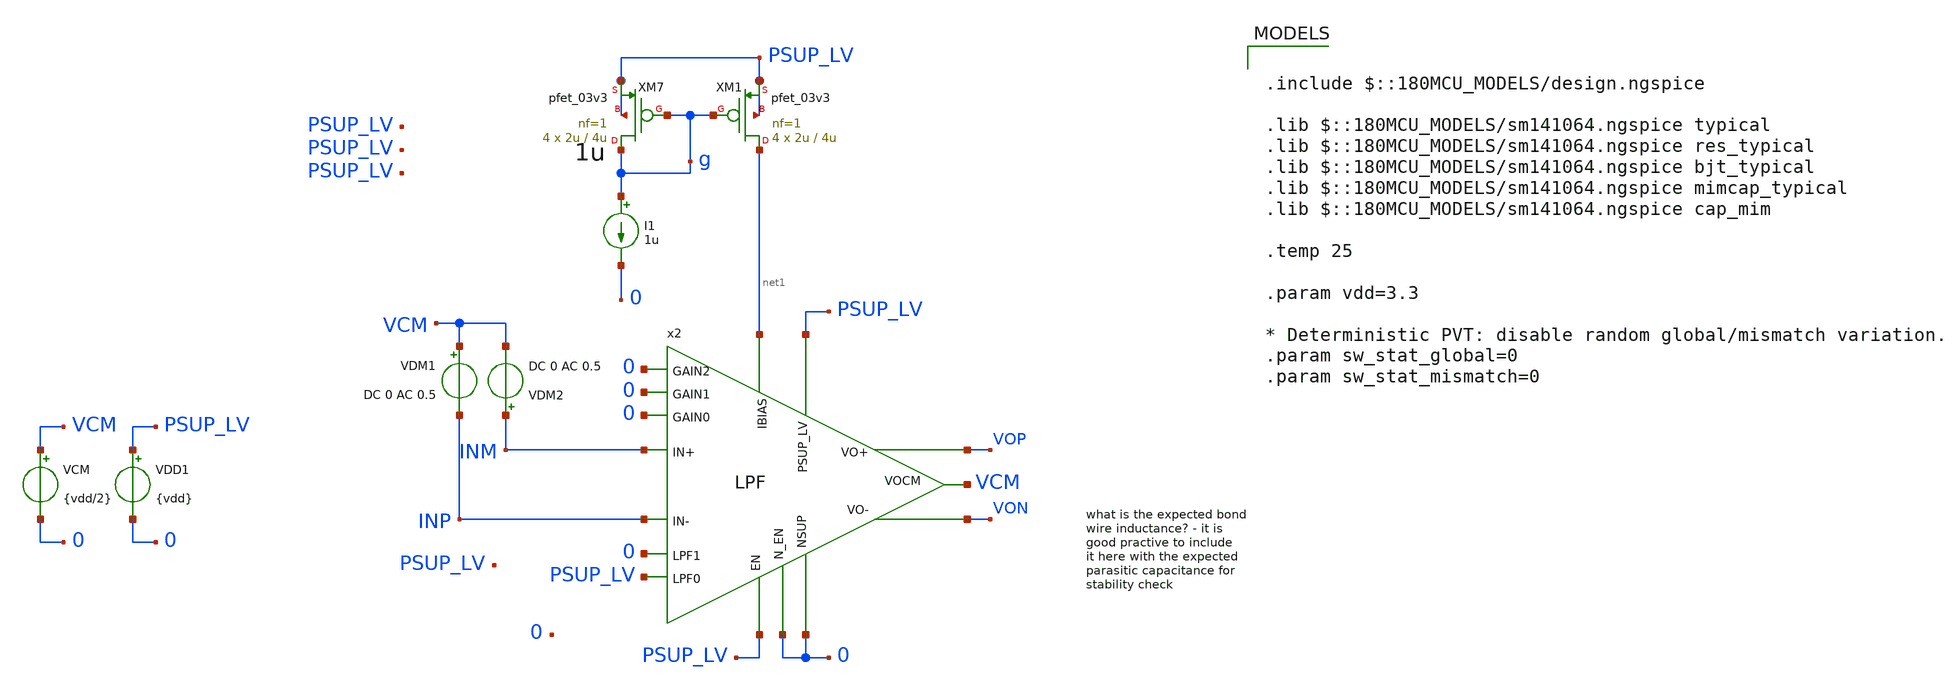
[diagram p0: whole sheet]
** sch_path: xschem/blocks/LPF/tb_LPF_gain.sch
**.subckt tb_LPF_gain
VDD1 PSUP_LV 0 {vdd}
VCM VCM 0 {vdd/2}
VDM2 INM VCM DC 0 AC 0.5
VDM1 VCM INP DC 0 AC 0.5
x2 PSUP_LV 0 PSUP_LV 0 net1 0 0 0 0 PSUP_LV INM VOP VCM INP VON LPF
XM7 g g PSUP_LV PSUP_LV pfet_03v3 L=4u W=2u nf=1 ad='int((nf+1)/2) * W/nf * 0.18u' as='int((nf+2)/2) * W/nf * 0.18u'
+ pd='2*int((nf+1)/2) * (W/nf + 0.18u)' ps='2*int((nf+2)/2) * (W/nf + 0.18u)' nrd='0.18u / W' nrs='0.18u / W'
+ sa=0 sb=0 sd=0 m=4
XM1 net1 g PSUP_LV PSUP_LV pfet_03v3 L=4u W=2u nf=1 ad='int((nf+1)/2) * W/nf * 0.18u' as='int((nf+2)/2) * W/nf * 0.18u'
+ pd='2*int((nf+1)/2) * (W/nf + 0.18u)' ps='2*int((nf+2)/2) * (W/nf + 0.18u)' nrd='0.18u / W' nrs='0.18u / W'
+ sa=0 sb=0 sd=0 m=4
I1 g 0 1u
**** begin user architecture code

.include $::180MCU_MODELS/design.ngspice

.lib $::180MCU_MODELS/sm141064.ngspice typical
.lib $::180MCU_MODELS/sm141064.ngspice res_typical
.lib $::180MCU_MODELS/sm141064.ngspice bjt_typical
.lib $::180MCU_MODELS/sm141064.ngspice mimcap_typical
.lib $::180MCU_MODELS/sm141064.ngspice cap_mim

.temp 25

.param vdd=3.3

* Deterministic PVT: disable random global/mismatch variation.
.param sw_stat_global=0
.param sw_stat_mismatch=0



.control
set units=degrees
save all
ac dec 100 1 1G

let Vid = v(INP) - v(INM)
let Vo = v(Vop) - v(Von)
let aol = v(Vo) / v(Vid)
let gain_db = db(aol)
let phase_deg = cph(aol)

write tb_LPF_gain.raw frequency v(Vop) v(Von) v(Vo) aol gain_db phase_deg

.endc


**** end user architecture code
**.ends
.end
